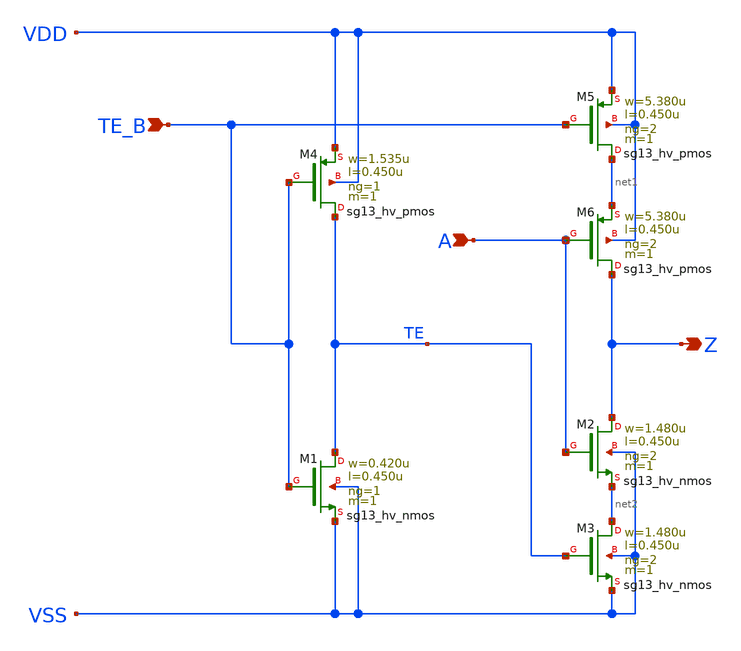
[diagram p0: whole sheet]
** sch_path: ihp-sg13g2/libs.ref/sg13g2_stdcell_hv/sch/xschem/sg13g2_hv_einvn_2.sch
* Copyright 2023 IHP PDK Authors
* Licensed under the Apache License, Version 2.0 (the "License");
* you may not use this file except in compliance with the License.
* You may obtain a copy of the License at
* https://www.apache.org/licenses/LICENSE-2.0
* Unless required by applicable law or agreed to in writing, software
* distributed under the License is distributed on an "AS IS" BASIS,
* WITHOUT WARRANTIES OR CONDITIONS OF ANY KIND, either express or implied.
* See the License for the specific language governing permissions and
* limitations under the License.
**.subckt sg13g2_hv_einvn_2 TE_B A Z
*.ipin TE_B
*.ipin A
*.opin Z
XM1 TE TE_B VSS VSS sg13_hv_nmos w=0.420u l=0.450u ng=1 m=1 mm_ok=1
XM2 Z A net2 VSS sg13_hv_nmos w=1.480u l=0.450u ng=2 m=1 mm_ok=1
XM3 net2 TE VSS VSS sg13_hv_nmos w=1.480u l=0.450u ng=2 m=1 mm_ok=1
XM4 TE TE_B VDD VDD sg13_hv_pmos w=1.535u l=0.450u ng=1 m=1 mm_ok=1
XM5 net1 TE_B VDD VDD sg13_hv_pmos w=5.380u l=0.450u ng=2 m=1 mm_ok=1
XM6 Z A net1 VDD sg13_hv_pmos w=5.380u l=0.450u ng=2 m=1 mm_ok=1
**.ends
.end
